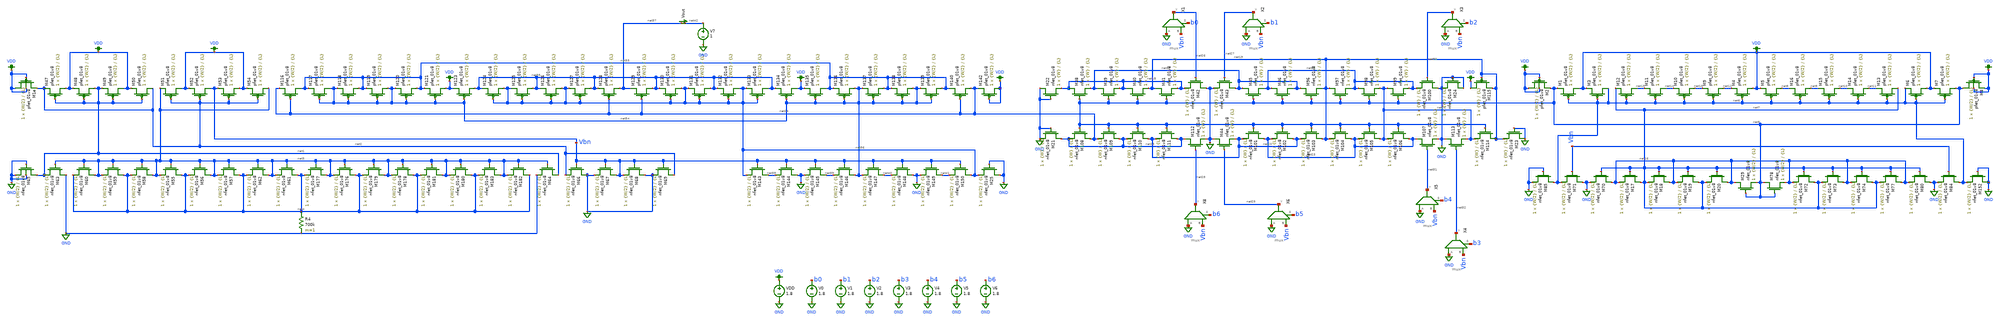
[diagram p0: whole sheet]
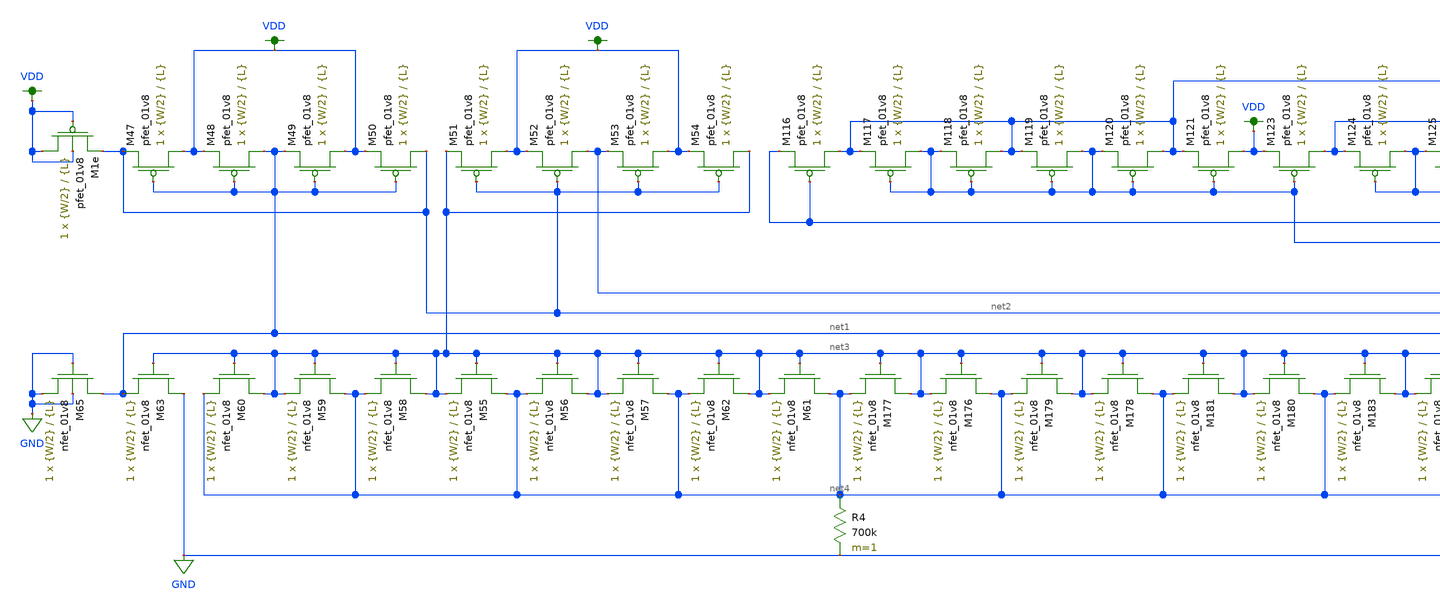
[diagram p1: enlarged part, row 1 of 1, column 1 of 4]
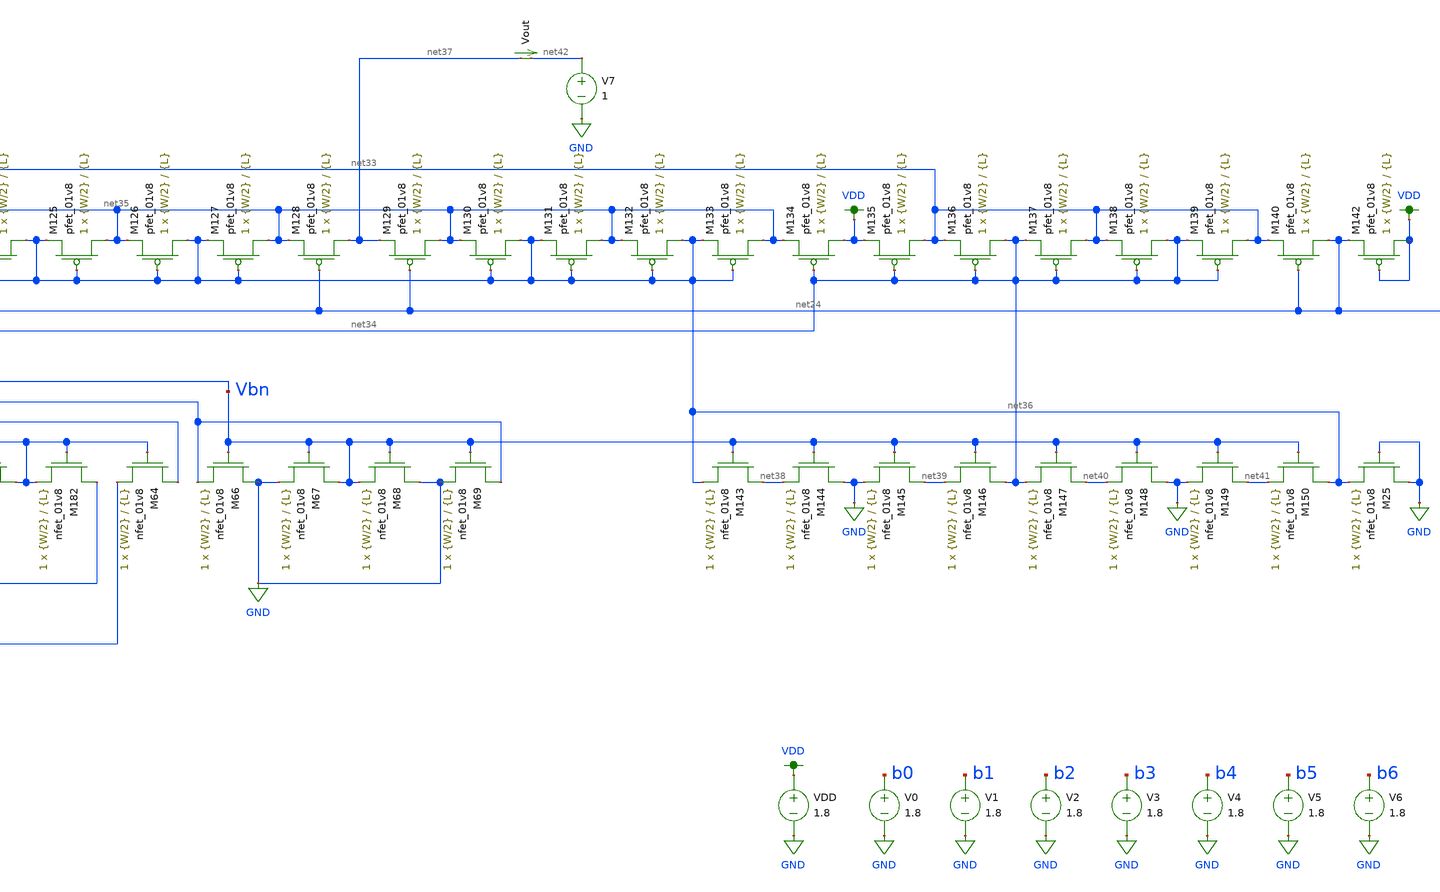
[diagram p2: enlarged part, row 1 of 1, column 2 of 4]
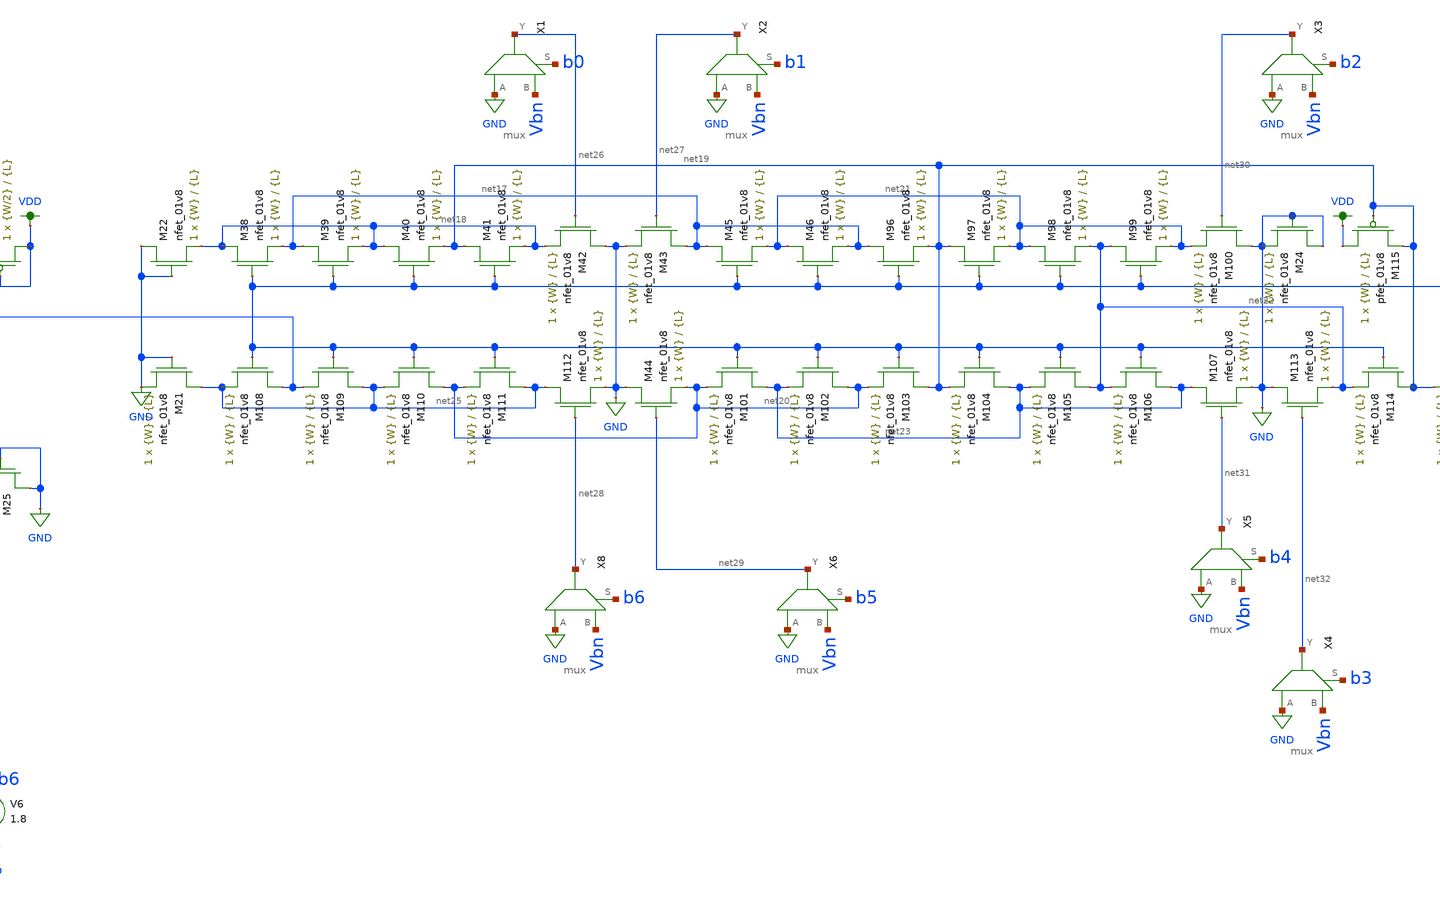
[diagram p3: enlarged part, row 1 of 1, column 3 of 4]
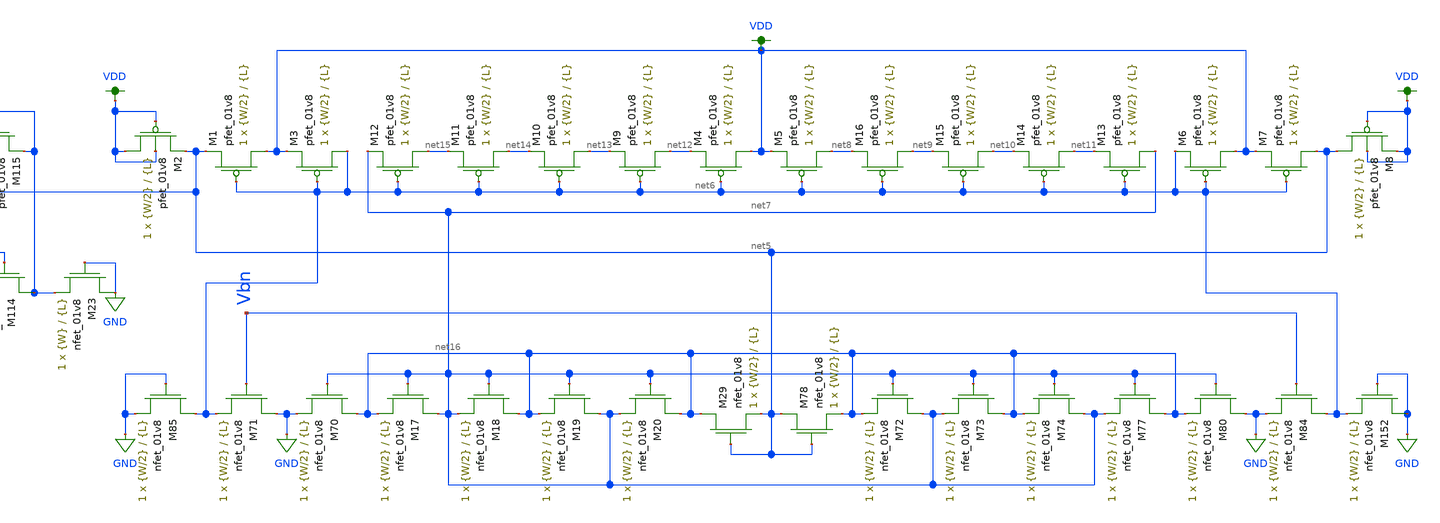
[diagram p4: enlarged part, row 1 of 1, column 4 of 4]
** sch_path: dac/schematics/LDS_FINAL.sch
**.subckt LDS_FINAL
V0 b0 GND 1.8
V1 b1 GND 1.8
V2 b2 GND 1.8
V3 b3 GND 1.8
V4 b4 GND 1.8
V5 b5 GND 1.8
V6 b6 GND 1.8
VDD VDD GND 1.8
XM47 VDD net1 net2 VDD sky130_fd_pr__pfet_01v8 L={L} W={W/2} nf=1 ad='int((nf+1)/2) * W/nf * 0.29' as='int((nf+2)/2) * W/nf * 0.29'
+ pd='2*int((nf+1)/2) * (W/nf + 0.29)' ps='2*int((nf+2)/2) * (W/nf + 0.29)' nrd='0.29 / W' nrs='0.29 / W'
+ sa=0 sb=0 sd=0 mult=1 m=1
XM48 net1 net1 VDD VDD sky130_fd_pr__pfet_01v8 L={L} W={W/2} nf=1 ad='int((nf+1)/2) * W/nf * 0.29' as='int((nf+2)/2) * W/nf * 0.29'
+ pd='2*int((nf+1)/2) * (W/nf + 0.29)' ps='2*int((nf+2)/2) * (W/nf + 0.29)' nrd='0.29 / W' nrs='0.29 / W'
+ sa=0 sb=0 sd=0 mult=1 m=1
XM49 VDD net1 net1 VDD sky130_fd_pr__pfet_01v8 L={L} W={W/2} nf=1 ad='int((nf+1)/2) * W/nf * 0.29' as='int((nf+2)/2) * W/nf * 0.29'
+ pd='2*int((nf+1)/2) * (W/nf + 0.29)' ps='2*int((nf+2)/2) * (W/nf + 0.29)' nrd='0.29 / W' nrs='0.29 / W'
+ sa=0 sb=0 sd=0 mult=1 m=1
XM50 net2 net1 VDD VDD sky130_fd_pr__pfet_01v8 L={L} W={W/2} nf=1 ad='int((nf+1)/2) * W/nf * 0.29' as='int((nf+2)/2) * W/nf * 0.29'
+ pd='2*int((nf+1)/2) * (W/nf + 0.29)' ps='2*int((nf+2)/2) * (W/nf + 0.29)' nrd='0.29 / W' nrs='0.29 / W'
+ sa=0 sb=0 sd=0 mult=1 m=1
XM51 VDD net2 net3 VDD sky130_fd_pr__pfet_01v8 L={L} W={W/2} nf=1 ad='int((nf+1)/2) * W/nf * 0.29' as='int((nf+2)/2) * W/nf * 0.29'
+ pd='2*int((nf+1)/2) * (W/nf + 0.29)' ps='2*int((nf+2)/2) * (W/nf + 0.29)' nrd='0.29 / W' nrs='0.29 / W'
+ sa=0 sb=0 sd=0 mult=1 m=1
XM52 Vbn net2 VDD VDD sky130_fd_pr__pfet_01v8 L={L} W={W/2} nf=1 ad='int((nf+1)/2) * W/nf * 0.29' as='int((nf+2)/2) * W/nf * 0.29'
+ pd='2*int((nf+1)/2) * (W/nf + 0.29)' ps='2*int((nf+2)/2) * (W/nf + 0.29)' nrd='0.29 / W' nrs='0.29 / W'
+ sa=0 sb=0 sd=0 mult=1 m=1
XM53 VDD net2 Vbn VDD sky130_fd_pr__pfet_01v8 L={L} W={W/2} nf=1 ad='int((nf+1)/2) * W/nf * 0.29' as='int((nf+2)/2) * W/nf * 0.29'
+ pd='2*int((nf+1)/2) * (W/nf + 0.29)' ps='2*int((nf+2)/2) * (W/nf + 0.29)' nrd='0.29 / W' nrs='0.29 / W'
+ sa=0 sb=0 sd=0 mult=1 m=1
XM54 net3 net2 VDD VDD sky130_fd_pr__pfet_01v8 L={L} W={W/2} nf=1 ad='int((nf+1)/2) * W/nf * 0.29' as='int((nf+2)/2) * W/nf * 0.29'
+ pd='2*int((nf+1)/2) * (W/nf + 0.29)' ps='2*int((nf+2)/2) * (W/nf + 0.29)' nrd='0.29 / W' nrs='0.29 / W'
+ sa=0 sb=0 sd=0 mult=1 m=1
XM55 net4 net3 net3 GND sky130_fd_pr__nfet_01v8 L={L} W={W/2} nf=1 ad='int((nf+1)/2) * W/nf * 0.29' as='int((nf+2)/2) * W/nf * 0.29'
+ pd='2*int((nf+1)/2) * (W/nf + 0.29)' ps='2*int((nf+2)/2) * (W/nf + 0.29)' nrd='0.29 / W' nrs='0.29 / W'
+ sa=0 sb=0 sd=0 mult=1 m=1
XM56 net3 net3 net4 GND sky130_fd_pr__nfet_01v8 L={L} W={W/2} nf=1 ad='int((nf+1)/2) * W/nf * 0.29' as='int((nf+2)/2) * W/nf * 0.29'
+ pd='2*int((nf+1)/2) * (W/nf + 0.29)' ps='2*int((nf+2)/2) * (W/nf + 0.29)' nrd='0.29 / W' nrs='0.29 / W'
+ sa=0 sb=0 sd=0 mult=1 m=1
XM57 net4 net3 net3 GND sky130_fd_pr__nfet_01v8 L={L} W={W/2} nf=1 ad='int((nf+1)/2) * W/nf * 0.29' as='int((nf+2)/2) * W/nf * 0.29'
+ pd='2*int((nf+1)/2) * (W/nf + 0.29)' ps='2*int((nf+2)/2) * (W/nf + 0.29)' nrd='0.29 / W' nrs='0.29 / W'
+ sa=0 sb=0 sd=0 mult=1 m=1
XM58 net3 net3 net4 GND sky130_fd_pr__nfet_01v8 L={L} W={W/2} nf=1 ad='int((nf+1)/2) * W/nf * 0.29' as='int((nf+2)/2) * W/nf * 0.29'
+ pd='2*int((nf+1)/2) * (W/nf + 0.29)' ps='2*int((nf+2)/2) * (W/nf + 0.29)' nrd='0.29 / W' nrs='0.29 / W'
+ sa=0 sb=0 sd=0 mult=1 m=1
XM59 net4 net3 net3 GND sky130_fd_pr__nfet_01v8 L={L} W={W/2} nf=1 ad='int((nf+1)/2) * W/nf * 0.29' as='int((nf+2)/2) * W/nf * 0.29'
+ pd='2*int((nf+1)/2) * (W/nf + 0.29)' ps='2*int((nf+2)/2) * (W/nf + 0.29)' nrd='0.29 / W' nrs='0.29 / W'
+ sa=0 sb=0 sd=0 mult=1 m=1
XM60 net3 net3 net4 GND sky130_fd_pr__nfet_01v8 L={L} W={W/2} nf=1 ad='int((nf+1)/2) * W/nf * 0.29' as='int((nf+2)/2) * W/nf * 0.29'
+ pd='2*int((nf+1)/2) * (W/nf + 0.29)' ps='2*int((nf+2)/2) * (W/nf + 0.29)' nrd='0.29 / W' nrs='0.29 / W'
+ sa=0 sb=0 sd=0 mult=1 m=1
XM61 net4 net3 net3 GND sky130_fd_pr__nfet_01v8 L={L} W={W/2} nf=1 ad='int((nf+1)/2) * W/nf * 0.29' as='int((nf+2)/2) * W/nf * 0.29'
+ pd='2*int((nf+1)/2) * (W/nf + 0.29)' ps='2*int((nf+2)/2) * (W/nf + 0.29)' nrd='0.29 / W' nrs='0.29 / W'
+ sa=0 sb=0 sd=0 mult=1 m=1
XM62 net3 net3 net4 GND sky130_fd_pr__nfet_01v8 L={L} W={W/2} nf=1 ad='int((nf+1)/2) * W/nf * 0.29' as='int((nf+2)/2) * W/nf * 0.29'
+ pd='2*int((nf+1)/2) * (W/nf + 0.29)' ps='2*int((nf+2)/2) * (W/nf + 0.29)' nrd='0.29 / W' nrs='0.29 / W'
+ sa=0 sb=0 sd=0 mult=1 m=1
XM63 GND net3 net1 GND sky130_fd_pr__nfet_01v8 L={L} W={W/2} nf=1 ad='int((nf+1)/2) * W/nf * 0.29' as='int((nf+2)/2) * W/nf * 0.29'
+ pd='2*int((nf+1)/2) * (W/nf + 0.29)' ps='2*int((nf+2)/2) * (W/nf + 0.29)' nrd='0.29 / W' nrs='0.29 / W'
+ sa=0 sb=0 sd=0 mult=1 m=1
XM64 net1 net3 GND GND sky130_fd_pr__nfet_01v8 L={L} W={W/2} nf=1 ad='int((nf+1)/2) * W/nf * 0.29' as='int((nf+2)/2) * W/nf * 0.29'
+ pd='2*int((nf+1)/2) * (W/nf + 0.29)' ps='2*int((nf+2)/2) * (W/nf + 0.29)' nrd='0.29 / W' nrs='0.29 / W'
+ sa=0 sb=0 sd=0 mult=1 m=1
R4 net4 GND 700k m=1
XM1e VDD VDD net2 VDD sky130_fd_pr__pfet_01v8 L={L} W={W/2} nf=1 ad='int((nf+1)/2) * W/nf * 0.29' as='int((nf+2)/2) * W/nf * 0.29'
+ pd='2*int((nf+1)/2) * (W/nf + 0.29)' ps='2*int((nf+2)/2) * (W/nf + 0.29)' nrd='0.29 / W' nrs='0.29 / W'
+ sa=0 sb=0 sd=0 mult=1 m=1
XM65 net1 GND GND GND sky130_fd_pr__nfet_01v8 L={L} W={W/2} nf=1 ad='int((nf+1)/2) * W/nf * 0.29' as='int((nf+2)/2) * W/nf * 0.29'
+ pd='2*int((nf+1)/2) * (W/nf + 0.29)' ps='2*int((nf+2)/2) * (W/nf + 0.29)' nrd='0.29 / W' nrs='0.29 / W'
+ sa=0 sb=0 sd=0 mult=1 m=1
XM66 GND Vbn net2 GND sky130_fd_pr__nfet_01v8 L={L} W={W/2} nf=1 ad='int((nf+1)/2) * W/nf * 0.29' as='int((nf+2)/2) * W/nf * 0.29'
+ pd='2*int((nf+1)/2) * (W/nf + 0.29)' ps='2*int((nf+2)/2) * (W/nf + 0.29)' nrd='0.29 / W' nrs='0.29 / W'
+ sa=0 sb=0 sd=0 mult=1 m=1
XM67 Vbn Vbn GND GND sky130_fd_pr__nfet_01v8 L={L} W={W/2} nf=1 ad='int((nf+1)/2) * W/nf * 0.29' as='int((nf+2)/2) * W/nf * 0.29'
+ pd='2*int((nf+1)/2) * (W/nf + 0.29)' ps='2*int((nf+2)/2) * (W/nf + 0.29)' nrd='0.29 / W' nrs='0.29 / W'
+ sa=0 sb=0 sd=0 mult=1 m=1
XM68 GND Vbn Vbn GND sky130_fd_pr__nfet_01v8 L={L} W={W/2} nf=1 ad='int((nf+1)/2) * W/nf * 0.29' as='int((nf+2)/2) * W/nf * 0.29'
+ pd='2*int((nf+1)/2) * (W/nf + 0.29)' ps='2*int((nf+2)/2) * (W/nf + 0.29)' nrd='0.29 / W' nrs='0.29 / W'
+ sa=0 sb=0 sd=0 mult=1 m=1
XM69 net2 Vbn GND GND sky130_fd_pr__nfet_01v8 L={L} W={W/2} nf=1 ad='int((nf+1)/2) * W/nf * 0.29' as='int((nf+2)/2) * W/nf * 0.29'
+ pd='2*int((nf+1)/2) * (W/nf + 0.29)' ps='2*int((nf+2)/2) * (W/nf + 0.29)' nrd='0.29 / W' nrs='0.29 / W'
+ sa=0 sb=0 sd=0 mult=1 m=1
XM176 net4 net3 net3 GND sky130_fd_pr__nfet_01v8 L={L} W={W/2} nf=1 ad='int((nf+1)/2) * W/nf * 0.29'
+ as='int((nf+2)/2) * W/nf * 0.29' pd='2*int((nf+1)/2) * (W/nf + 0.29)' ps='2*int((nf+2)/2) * (W/nf + 0.29)'
+ nrd='0.29 / W' nrs='0.29 / W' sa=0 sb=0 sd=0 mult=1 m=1
XM177 net3 net3 net4 GND sky130_fd_pr__nfet_01v8 L={L} W={W/2} nf=1 ad='int((nf+1)/2) * W/nf * 0.29'
+ as='int((nf+2)/2) * W/nf * 0.29' pd='2*int((nf+1)/2) * (W/nf + 0.29)' ps='2*int((nf+2)/2) * (W/nf + 0.29)'
+ nrd='0.29 / W' nrs='0.29 / W' sa=0 sb=0 sd=0 mult=1 m=1
XM178 net4 net3 net3 GND sky130_fd_pr__nfet_01v8 L={L} W={W/2} nf=1 ad='int((nf+1)/2) * W/nf * 0.29'
+ as='int((nf+2)/2) * W/nf * 0.29' pd='2*int((nf+1)/2) * (W/nf + 0.29)' ps='2*int((nf+2)/2) * (W/nf + 0.29)'
+ nrd='0.29 / W' nrs='0.29 / W' sa=0 sb=0 sd=0 mult=1 m=1
XM179 net3 net3 net4 GND sky130_fd_pr__nfet_01v8 L={L} W={W/2} nf=1 ad='int((nf+1)/2) * W/nf * 0.29'
+ as='int((nf+2)/2) * W/nf * 0.29' pd='2*int((nf+1)/2) * (W/nf + 0.29)' ps='2*int((nf+2)/2) * (W/nf + 0.29)'
+ nrd='0.29 / W' nrs='0.29 / W' sa=0 sb=0 sd=0 mult=1 m=1
XM180 net4 net3 net3 GND sky130_fd_pr__nfet_01v8 L={L} W={W/2} nf=1 ad='int((nf+1)/2) * W/nf * 0.29'
+ as='int((nf+2)/2) * W/nf * 0.29' pd='2*int((nf+1)/2) * (W/nf + 0.29)' ps='2*int((nf+2)/2) * (W/nf + 0.29)'
+ nrd='0.29 / W' nrs='0.29 / W' sa=0 sb=0 sd=0 mult=1 m=1
XM181 net3 net3 net4 GND sky130_fd_pr__nfet_01v8 L={L} W={W/2} nf=1 ad='int((nf+1)/2) * W/nf * 0.29'
+ as='int((nf+2)/2) * W/nf * 0.29' pd='2*int((nf+1)/2) * (W/nf + 0.29)' ps='2*int((nf+2)/2) * (W/nf + 0.29)'
+ nrd='0.29 / W' nrs='0.29 / W' sa=0 sb=0 sd=0 mult=1 m=1
XM182 net4 net3 net3 GND sky130_fd_pr__nfet_01v8 L={L} W={W/2} nf=1 ad='int((nf+1)/2) * W/nf * 0.29'
+ as='int((nf+2)/2) * W/nf * 0.29' pd='2*int((nf+1)/2) * (W/nf + 0.29)' ps='2*int((nf+2)/2) * (W/nf + 0.29)'
+ nrd='0.29 / W' nrs='0.29 / W' sa=0 sb=0 sd=0 mult=1 m=1
XM183 net3 net3 net4 GND sky130_fd_pr__nfet_01v8 L={L} W={W/2} nf=1 ad='int((nf+1)/2) * W/nf * 0.29'
+ as='int((nf+2)/2) * W/nf * 0.29' pd='2*int((nf+1)/2) * (W/nf + 0.29)' ps='2*int((nf+2)/2) * (W/nf + 0.29)'
+ nrd='0.29 / W' nrs='0.29 / W' sa=0 sb=0 sd=0 mult=1 m=1
XM1 VDD net6 net5 VDD sky130_fd_pr__pfet_01v8 L={L} W={W/2} nf=1 ad='int((nf+1)/2) * W/nf * 0.29' as='int((nf+2)/2) * W/nf * 0.29'
+ pd='2*int((nf+1)/2) * (W/nf + 0.29)' ps='2*int((nf+2)/2) * (W/nf + 0.29)' nrd='0.29 / W' nrs='0.29 / W'
+ sa=0 sb=0 sd=0 mult=1 m=1
XM2 VDD VDD net5 VDD sky130_fd_pr__pfet_01v8 L={L} W={W/2} nf=1 ad='int((nf+1)/2) * W/nf * 0.29' as='int((nf+2)/2) * W/nf * 0.29'
+ pd='2*int((nf+1)/2) * (W/nf + 0.29)' ps='2*int((nf+2)/2) * (W/nf + 0.29)' nrd='0.29 / W' nrs='0.29 / W'
+ sa=0 sb=0 sd=0 mult=1 m=1
XM3 net6 net6 VDD VDD sky130_fd_pr__pfet_01v8 L={L} W={W/2} nf=1 ad='int((nf+1)/2) * W/nf * 0.29' as='int((nf+2)/2) * W/nf * 0.29'
+ pd='2*int((nf+1)/2) * (W/nf + 0.29)' ps='2*int((nf+2)/2) * (W/nf + 0.29)' nrd='0.29 / W' nrs='0.29 / W'
+ sa=0 sb=0 sd=0 mult=1 m=1
XM4 VDD net6 net12 VDD sky130_fd_pr__pfet_01v8 L={L} W={W/2} nf=1 ad='int((nf+1)/2) * W/nf * 0.29' as='int((nf+2)/2) * W/nf * 0.29'
+ pd='2*int((nf+1)/2) * (W/nf + 0.29)' ps='2*int((nf+2)/2) * (W/nf + 0.29)' nrd='0.29 / W' nrs='0.29 / W'
+ sa=0 sb=0 sd=0 mult=1 m=1
XM5 net8 net6 VDD VDD sky130_fd_pr__pfet_01v8 L={L} W={W/2} nf=1 ad='int((nf+1)/2) * W/nf * 0.29' as='int((nf+2)/2) * W/nf * 0.29'
+ pd='2*int((nf+1)/2) * (W/nf + 0.29)' ps='2*int((nf+2)/2) * (W/nf + 0.29)' nrd='0.29 / W' nrs='0.29 / W'
+ sa=0 sb=0 sd=0 mult=1 m=1
XM6 VDD net6 net6 VDD sky130_fd_pr__pfet_01v8 L={L} W={W/2} nf=1 ad='int((nf+1)/2) * W/nf * 0.29' as='int((nf+2)/2) * W/nf * 0.29'
+ pd='2*int((nf+1)/2) * (W/nf + 0.29)' ps='2*int((nf+2)/2) * (W/nf + 0.29)' nrd='0.29 / W' nrs='0.29 / W'
+ sa=0 sb=0 sd=0 mult=1 m=1
XM7 net5 net6 VDD VDD sky130_fd_pr__pfet_01v8 L={L} W={W/2} nf=1 ad='int((nf+1)/2) * W/nf * 0.29' as='int((nf+2)/2) * W/nf * 0.29'
+ pd='2*int((nf+1)/2) * (W/nf + 0.29)' ps='2*int((nf+2)/2) * (W/nf + 0.29)' nrd='0.29 / W' nrs='0.29 / W'
+ sa=0 sb=0 sd=0 mult=1 m=1
XM8 net5 VDD VDD VDD sky130_fd_pr__pfet_01v8 L={L} W={W/2} nf=1 ad='int((nf+1)/2) * W/nf * 0.29' as='int((nf+2)/2) * W/nf * 0.29'
+ pd='2*int((nf+1)/2) * (W/nf + 0.29)' ps='2*int((nf+2)/2) * (W/nf + 0.29)' nrd='0.29 / W' nrs='0.29 / W'
+ sa=0 sb=0 sd=0 mult=1 m=1
XM9 net12 net6 net13 VDD sky130_fd_pr__pfet_01v8 L={L} W={W/2} nf=1 ad='int((nf+1)/2) * W/nf * 0.29'
+ as='int((nf+2)/2) * W/nf * 0.29' pd='2*int((nf+1)/2) * (W/nf + 0.29)' ps='2*int((nf+2)/2) * (W/nf + 0.29)'
+ nrd='0.29 / W' nrs='0.29 / W' sa=0 sb=0 sd=0 mult=1 m=1
XM10 net13 net6 net14 VDD sky130_fd_pr__pfet_01v8 L={L} W={W/2} nf=1 ad='int((nf+1)/2) * W/nf * 0.29'
+ as='int((nf+2)/2) * W/nf * 0.29' pd='2*int((nf+1)/2) * (W/nf + 0.29)' ps='2*int((nf+2)/2) * (W/nf + 0.29)'
+ nrd='0.29 / W' nrs='0.29 / W' sa=0 sb=0 sd=0 mult=1 m=1
XM11 net14 net6 net15 VDD sky130_fd_pr__pfet_01v8 L={L} W={W/2} nf=1 ad='int((nf+1)/2) * W/nf * 0.29'
+ as='int((nf+2)/2) * W/nf * 0.29' pd='2*int((nf+1)/2) * (W/nf + 0.29)' ps='2*int((nf+2)/2) * (W/nf + 0.29)'
+ nrd='0.29 / W' nrs='0.29 / W' sa=0 sb=0 sd=0 mult=1 m=1
XM12 net15 net6 net7 VDD sky130_fd_pr__pfet_01v8 L={L} W={W/2} nf=1 ad='int((nf+1)/2) * W/nf * 0.29'
+ as='int((nf+2)/2) * W/nf * 0.29' pd='2*int((nf+1)/2) * (W/nf + 0.29)' ps='2*int((nf+2)/2) * (W/nf + 0.29)'
+ nrd='0.29 / W' nrs='0.29 / W' sa=0 sb=0 sd=0 mult=1 m=1
XM13 net7 net6 net11 VDD sky130_fd_pr__pfet_01v8 L={L} W={W/2} nf=1 ad='int((nf+1)/2) * W/nf * 0.29'
+ as='int((nf+2)/2) * W/nf * 0.29' pd='2*int((nf+1)/2) * (W/nf + 0.29)' ps='2*int((nf+2)/2) * (W/nf + 0.29)'
+ nrd='0.29 / W' nrs='0.29 / W' sa=0 sb=0 sd=0 mult=1 m=1
XM14 net11 net6 net10 VDD sky130_fd_pr__pfet_01v8 L={L} W={W/2} nf=1 ad='int((nf+1)/2) * W/nf * 0.29'
+ as='int((nf+2)/2) * W/nf * 0.29' pd='2*int((nf+1)/2) * (W/nf + 0.29)' ps='2*int((nf+2)/2) * (W/nf + 0.29)'
+ nrd='0.29 / W' nrs='0.29 / W' sa=0 sb=0 sd=0 mult=1 m=1
XM15 net10 net6 net9 VDD sky130_fd_pr__pfet_01v8 L={L} W={W/2} nf=1 ad='int((nf+1)/2) * W/nf * 0.29'
+ as='int((nf+2)/2) * W/nf * 0.29' pd='2*int((nf+1)/2) * (W/nf + 0.29)' ps='2*int((nf+2)/2) * (W/nf + 0.29)'
+ nrd='0.29 / W' nrs='0.29 / W' sa=0 sb=0 sd=0 mult=1 m=1
XM16 net9 net6 net8 VDD sky130_fd_pr__pfet_01v8 L={L} W={W/2} nf=1 ad='int((nf+1)/2) * W/nf * 0.29' as='int((nf+2)/2) * W/nf * 0.29'
+ pd='2*int((nf+1)/2) * (W/nf + 0.29)' ps='2*int((nf+2)/2) * (W/nf + 0.29)' nrd='0.29 / W' nrs='0.29 / W'
+ sa=0 sb=0 sd=0 mult=1 m=1
XM17 net7 net7 net16 GND sky130_fd_pr__nfet_01v8 L={L} W={W/2} nf=1 ad='int((nf+1)/2) * W/nf * 0.29'
+ as='int((nf+2)/2) * W/nf * 0.29' pd='2*int((nf+1)/2) * (W/nf + 0.29)' ps='2*int((nf+2)/2) * (W/nf + 0.29)'
+ nrd='0.29 / W' nrs='0.29 / W' sa=0 sb=0 sd=0 mult=1 m=1
XM18 net16 net7 net7 GND sky130_fd_pr__nfet_01v8 L={L} W={W/2} nf=1 ad='int((nf+1)/2) * W/nf * 0.29'
+ as='int((nf+2)/2) * W/nf * 0.29' pd='2*int((nf+1)/2) * (W/nf + 0.29)' ps='2*int((nf+2)/2) * (W/nf + 0.29)'
+ nrd='0.29 / W' nrs='0.29 / W' sa=0 sb=0 sd=0 mult=1 m=1
XM19 net7 net7 net16 GND sky130_fd_pr__nfet_01v8 L={L} W={W/2} nf=1 ad='int((nf+1)/2) * W/nf * 0.29'
+ as='int((nf+2)/2) * W/nf * 0.29' pd='2*int((nf+1)/2) * (W/nf + 0.29)' ps='2*int((nf+2)/2) * (W/nf + 0.29)'
+ nrd='0.29 / W' nrs='0.29 / W' sa=0 sb=0 sd=0 mult=1 m=1
XM20 net16 net7 net7 GND sky130_fd_pr__nfet_01v8 L={L} W={W/2} nf=1 ad='int((nf+1)/2) * W/nf * 0.29'
+ as='int((nf+2)/2) * W/nf * 0.29' pd='2*int((nf+1)/2) * (W/nf + 0.29)' ps='2*int((nf+2)/2) * (W/nf + 0.29)'
+ nrd='0.29 / W' nrs='0.29 / W' sa=0 sb=0 sd=0 mult=1 m=1
XM29 net16 net5 net5 GND sky130_fd_pr__nfet_01v8 L={L} W={W/2} nf=1 ad='int((nf+1)/2) * W/nf * 0.29'
+ as='int((nf+2)/2) * W/nf * 0.29' pd='2*int((nf+1)/2) * (W/nf + 0.29)' ps='2*int((nf+2)/2) * (W/nf + 0.29)'
+ nrd='0.29 / W' nrs='0.29 / W' sa=0 sb=0 sd=0 mult=1 m=1
XM70 net16 net7 GND GND sky130_fd_pr__nfet_01v8 L={L} W={W/2} nf=1 ad='int((nf+1)/2) * W/nf * 0.29' as='int((nf+2)/2) * W/nf * 0.29'
+ pd='2*int((nf+1)/2) * (W/nf + 0.29)' ps='2*int((nf+2)/2) * (W/nf + 0.29)' nrd='0.29 / W' nrs='0.29 / W'
+ sa=0 sb=0 sd=0 mult=1 m=1
XM71 GND Vbn net6 GND sky130_fd_pr__nfet_01v8 L={L} W={W/2} nf=1 ad='int((nf+1)/2) * W/nf * 0.29' as='int((nf+2)/2) * W/nf * 0.29'
+ pd='2*int((nf+1)/2) * (W/nf + 0.29)' ps='2*int((nf+2)/2) * (W/nf + 0.29)' nrd='0.29 / W' nrs='0.29 / W'
+ sa=0 sb=0 sd=0 mult=1 m=1
XM72 net7 net7 net16 GND sky130_fd_pr__nfet_01v8 L={L} W={W/2} nf=1 ad='int((nf+1)/2) * W/nf * 0.29'
+ as='int((nf+2)/2) * W/nf * 0.29' pd='2*int((nf+1)/2) * (W/nf + 0.29)' ps='2*int((nf+2)/2) * (W/nf + 0.29)'
+ nrd='0.29 / W' nrs='0.29 / W' sa=0 sb=0 sd=0 mult=1 m=1
XM73 net16 net7 net7 GND sky130_fd_pr__nfet_01v8 L={L} W={W/2} nf=1 ad='int((nf+1)/2) * W/nf * 0.29'
+ as='int((nf+2)/2) * W/nf * 0.29' pd='2*int((nf+1)/2) * (W/nf + 0.29)' ps='2*int((nf+2)/2) * (W/nf + 0.29)'
+ nrd='0.29 / W' nrs='0.29 / W' sa=0 sb=0 sd=0 mult=1 m=1
XM74 net7 net7 net16 GND sky130_fd_pr__nfet_01v8 L={L} W={W/2} nf=1 ad='int((nf+1)/2) * W/nf * 0.29'
+ as='int((nf+2)/2) * W/nf * 0.29' pd='2*int((nf+1)/2) * (W/nf + 0.29)' ps='2*int((nf+2)/2) * (W/nf + 0.29)'
+ nrd='0.29 / W' nrs='0.29 / W' sa=0 sb=0 sd=0 mult=1 m=1
XM77 net16 net7 net7 GND sky130_fd_pr__nfet_01v8 L={L} W={W/2} nf=1 ad='int((nf+1)/2) * W/nf * 0.29'
+ as='int((nf+2)/2) * W/nf * 0.29' pd='2*int((nf+1)/2) * (W/nf + 0.29)' ps='2*int((nf+2)/2) * (W/nf + 0.29)'
+ nrd='0.29 / W' nrs='0.29 / W' sa=0 sb=0 sd=0 mult=1 m=1
XM78 net5 net5 net16 GND sky130_fd_pr__nfet_01v8 L={L} W={W/2} nf=1 ad='int((nf+1)/2) * W/nf * 0.29'
+ as='int((nf+2)/2) * W/nf * 0.29' pd='2*int((nf+1)/2) * (W/nf + 0.29)' ps='2*int((nf+2)/2) * (W/nf + 0.29)'
+ nrd='0.29 / W' nrs='0.29 / W' sa=0 sb=0 sd=0 mult=1 m=1
XM80 GND net7 net16 GND sky130_fd_pr__nfet_01v8 L={L} W={W/2} nf=1 ad='int((nf+1)/2) * W/nf * 0.29' as='int((nf+2)/2) * W/nf * 0.29'
+ pd='2*int((nf+1)/2) * (W/nf + 0.29)' ps='2*int((nf+2)/2) * (W/nf + 0.29)' nrd='0.29 / W' nrs='0.29 / W'
+ sa=0 sb=0 sd=0 mult=1 m=1
XM84 net6 Vbn GND GND sky130_fd_pr__nfet_01v8 L={L} W={W/2} nf=1 ad='int((nf+1)/2) * W/nf * 0.29' as='int((nf+2)/2) * W/nf * 0.29'
+ pd='2*int((nf+1)/2) * (W/nf + 0.29)' ps='2*int((nf+2)/2) * (W/nf + 0.29)' nrd='0.29 / W' nrs='0.29 / W'
+ sa=0 sb=0 sd=0 mult=1 m=1
XM85 net6 GND GND GND sky130_fd_pr__nfet_01v8 L={L} W={W/2} nf=1 ad='int((nf+1)/2) * W/nf * 0.29' as='int((nf+2)/2) * W/nf * 0.29'
+ pd='2*int((nf+1)/2) * (W/nf + 0.29)' ps='2*int((nf+2)/2) * (W/nf + 0.29)' nrd='0.29 / W' nrs='0.29 / W'
+ sa=0 sb=0 sd=0 mult=1 m=1
XM152 GND GND net6 GND sky130_fd_pr__nfet_01v8 L={L} W={W/2} nf=1 ad='int((nf+1)/2) * W/nf * 0.29' as='int((nf+2)/2) * W/nf * 0.29'
+ pd='2*int((nf+1)/2) * (W/nf + 0.29)' ps='2*int((nf+2)/2) * (W/nf + 0.29)' nrd='0.29 / W' nrs='0.29 / W'
+ sa=0 sb=0 sd=0 mult=1 m=1
X1 GND Vbn net26 b0 mux
X2 GND Vbn net27 b1 mux
X3 GND Vbn net30 b2 mux
X4 GND Vbn net32 b3 mux
X5 GND Vbn net31 b4 mux
X6 GND Vbn net29 b5 mux
X8 GND Vbn net28 b6 mux
XM38 net18 net5 net17 GND sky130_fd_pr__nfet_01v8 L={L} W={W} nf=1 ad='int((nf+1)/2) * W/nf * 0.29' as='int((nf+2)/2) * W/nf * 0.29'
+ pd='2*int((nf+1)/2) * (W/nf + 0.29)' ps='2*int((nf+2)/2) * (W/nf + 0.29)' nrd='0.29 / W' nrs='0.29 / W'
+ sa=0 sb=0 sd=0 mult=1 m=1
XM39 net17 net5 net18 GND sky130_fd_pr__nfet_01v8 L={L} W={W} nf=1 ad='int((nf+1)/2) * W/nf * 0.29' as='int((nf+2)/2) * W/nf * 0.29'
+ pd='2*int((nf+1)/2) * (W/nf + 0.29)' ps='2*int((nf+2)/2) * (W/nf + 0.29)' nrd='0.29 / W' nrs='0.29 / W'
+ sa=0 sb=0 sd=0 mult=1 m=1
XM40 net18 net5 net19 GND sky130_fd_pr__nfet_01v8 L={L} W={W} nf=1 ad='int((nf+1)/2) * W/nf * 0.29' as='int((nf+2)/2) * W/nf * 0.29'
+ pd='2*int((nf+1)/2) * (W/nf + 0.29)' ps='2*int((nf+2)/2) * (W/nf + 0.29)' nrd='0.29 / W' nrs='0.29 / W'
+ sa=0 sb=0 sd=0 mult=1 m=1
XM41 net19 net5 net18 GND sky130_fd_pr__nfet_01v8 L={L} W={W} nf=1 ad='int((nf+1)/2) * W/nf * 0.29' as='int((nf+2)/2) * W/nf * 0.29'
+ pd='2*int((nf+1)/2) * (W/nf + 0.29)' ps='2*int((nf+2)/2) * (W/nf + 0.29)' nrd='0.29 / W' nrs='0.29 / W'
+ sa=0 sb=0 sd=0 mult=1 m=1
XM42 GND net26 net18 GND sky130_fd_pr__nfet_01v8 L={L} W={W} nf=1 ad='int((nf+1)/2) * W/nf * 0.29' as='int((nf+2)/2) * W/nf * 0.29'
+ pd='2*int((nf+1)/2) * (W/nf + 0.29)' ps='2*int((nf+2)/2) * (W/nf + 0.29)' nrd='0.29 / W' nrs='0.29 / W'
+ sa=0 sb=0 sd=0 mult=1 m=1
XM43 net17 net27 GND GND sky130_fd_pr__nfet_01v8 L={L} W={W} nf=1 ad='int((nf+1)/2) * W/nf * 0.29' as='int((nf+2)/2) * W/nf * 0.29'
+ pd='2*int((nf+1)/2) * (W/nf + 0.29)' ps='2*int((nf+2)/2) * (W/nf + 0.29)' nrd='0.29 / W' nrs='0.29 / W'
+ sa=0 sb=0 sd=0 mult=1 m=1
XM44 GND net29 net20 GND sky130_fd_pr__nfet_01v8 L={L} W={W} nf=1 ad='int((nf+1)/2) * W/nf * 0.29' as='int((nf+2)/2) * W/nf * 0.29'
+ pd='2*int((nf+1)/2) * (W/nf + 0.29)' ps='2*int((nf+2)/2) * (W/nf + 0.29)' nrd='0.29 / W' nrs='0.29 / W'
+ sa=0 sb=0 sd=0 mult=1 m=1
XM45 net17 net5 net21 GND sky130_fd_pr__nfet_01v8 L={L} W={W} nf=1 ad='int((nf+1)/2) * W/nf * 0.29' as='int((nf+2)/2) * W/nf * 0.29'
+ pd='2*int((nf+1)/2) * (W/nf + 0.29)' ps='2*int((nf+2)/2) * (W/nf + 0.29)' nrd='0.29 / W' nrs='0.29 / W'
+ sa=0 sb=0 sd=0 mult=1 m=1
XM46 net21 net5 net17 GND sky130_fd_pr__nfet_01v8 L={L} W={W} nf=1 ad='int((nf+1)/2) * W/nf * 0.29' as='int((nf+2)/2) * W/nf * 0.29'
+ pd='2*int((nf+1)/2) * (W/nf + 0.29)' ps='2*int((nf+2)/2) * (W/nf + 0.29)' nrd='0.29 / W' nrs='0.29 / W'
+ sa=0 sb=0 sd=0 mult=1 m=1
XM96 net17 net5 net19 GND sky130_fd_pr__nfet_01v8 L={L} W={W} nf=1 ad='int((nf+1)/2) * W/nf * 0.29' as='int((nf+2)/2) * W/nf * 0.29'
+ pd='2*int((nf+1)/2) * (W/nf + 0.29)' ps='2*int((nf+2)/2) * (W/nf + 0.29)' nrd='0.29 / W' nrs='0.29 / W'
+ sa=0 sb=0 sd=0 mult=1 m=1
XM97 net19 net5 net21 GND sky130_fd_pr__nfet_01v8 L={L} W={W} nf=1 ad='int((nf+1)/2) * W/nf * 0.29' as='int((nf+2)/2) * W/nf * 0.29'
+ pd='2*int((nf+1)/2) * (W/nf + 0.29)' ps='2*int((nf+2)/2) * (W/nf + 0.29)' nrd='0.29 / W' nrs='0.29 / W'
+ sa=0 sb=0 sd=0 mult=1 m=1
XM98 net21 net5 net22 GND sky130_fd_pr__nfet_01v8 L={L} W={W} nf=1 ad='int((nf+1)/2) * W/nf * 0.29' as='int((nf+2)/2) * W/nf * 0.29'
+ pd='2*int((nf+1)/2) * (W/nf + 0.29)' ps='2*int((nf+2)/2) * (W/nf + 0.29)' nrd='0.29 / W' nrs='0.29 / W'
+ sa=0 sb=0 sd=0 mult=1 m=1
XM99 net22 net5 net21 GND sky130_fd_pr__nfet_01v8 L={L} W={W} nf=1 ad='int((nf+1)/2) * W/nf * 0.29' as='int((nf+2)/2) * W/nf * 0.29'
+ pd='2*int((nf+1)/2) * (W/nf + 0.29)' ps='2*int((nf+2)/2) * (W/nf + 0.29)' nrd='0.29 / W' nrs='0.29 / W'
+ sa=0 sb=0 sd=0 mult=1 m=1
XM100 GND net30 net21 GND sky130_fd_pr__nfet_01v8 L={L} W={W} nf=1 ad='int((nf+1)/2) * W/nf * 0.29' as='int((nf+2)/2) * W/nf * 0.29'
+ pd='2*int((nf+1)/2) * (W/nf + 0.29)' ps='2*int((nf+2)/2) * (W/nf + 0.29)' nrd='0.29 / W' nrs='0.29 / W'
+ sa=0 sb=0 sd=0 mult=1 m=1
XM101 net23 net5 net20 GND sky130_fd_pr__nfet_01v8 L={L} W={W} nf=1 ad='int((nf+1)/2) * W/nf * 0.29'
+ as='int((nf+2)/2) * W/nf * 0.29' pd='2*int((nf+1)/2) * (W/nf + 0.29)' ps='2*int((nf+2)/2) * (W/nf + 0.29)'
+ nrd='0.29 / W' nrs='0.29 / W' sa=0 sb=0 sd=0 mult=1 m=1
XM102 net20 net5 net23 GND sky130_fd_pr__nfet_01v8 L={L} W={W} nf=1 ad='int((nf+1)/2) * W/nf * 0.29'
+ as='int((nf+2)/2) * W/nf * 0.29' pd='2*int((nf+1)/2) * (W/nf + 0.29)' ps='2*int((nf+2)/2) * (W/nf + 0.29)'
+ nrd='0.29 / W' nrs='0.29 / W' sa=0 sb=0 sd=0 mult=1 m=1
XM103 net19 net5 net20 GND sky130_fd_pr__nfet_01v8 L={L} W={W} nf=1 ad='int((nf+1)/2) * W/nf * 0.29'
+ as='int((nf+2)/2) * W/nf * 0.29' pd='2*int((nf+1)/2) * (W/nf + 0.29)' ps='2*int((nf+2)/2) * (W/nf + 0.29)'
+ nrd='0.29 / W' nrs='0.29 / W' sa=0 sb=0 sd=0 mult=1 m=1
XM104 net23 net5 net19 GND sky130_fd_pr__nfet_01v8 L={L} W={W} nf=1 ad='int((nf+1)/2) * W/nf * 0.29'
+ as='int((nf+2)/2) * W/nf * 0.29' pd='2*int((nf+1)/2) * (W/nf + 0.29)' ps='2*int((nf+2)/2) * (W/nf + 0.29)'
+ nrd='0.29 / W' nrs='0.29 / W' sa=0 sb=0 sd=0 mult=1 m=1
XM105 net22 net5 net23 GND sky130_fd_pr__nfet_01v8 L={L} W={W} nf=1 ad='int((nf+1)/2) * W/nf * 0.29'
+ as='int((nf+2)/2) * W/nf * 0.29' pd='2*int((nf+1)/2) * (W/nf + 0.29)' ps='2*int((nf+2)/2) * (W/nf + 0.29)'
+ nrd='0.29 / W' nrs='0.29 / W' sa=0 sb=0 sd=0 mult=1 m=1
XM106 net23 net5 net22 GND sky130_fd_pr__nfet_01v8 L={L} W={W} nf=1 ad='int((nf+1)/2) * W/nf * 0.29'
+ as='int((nf+2)/2) * W/nf * 0.29' pd='2*int((nf+1)/2) * (W/nf + 0.29)' ps='2*int((nf+2)/2) * (W/nf + 0.29)'
+ nrd='0.29 / W' nrs='0.29 / W' sa=0 sb=0 sd=0 mult=1 m=1
XM107 net23 net31 GND GND sky130_fd_pr__nfet_01v8 L={L} W={W} nf=1 ad='int((nf+1)/2) * W/nf * 0.29' as='int((nf+2)/2) * W/nf * 0.29'
+ pd='2*int((nf+1)/2) * (W/nf + 0.29)' ps='2*int((nf+2)/2) * (W/nf + 0.29)' nrd='0.29 / W' nrs='0.29 / W'
+ sa=0 sb=0 sd=0 mult=1 m=1
XM108 net24 net5 net25 GND sky130_fd_pr__nfet_01v8 L={L} W={W} nf=1 ad='int((nf+1)/2) * W/nf * 0.29'
+ as='int((nf+2)/2) * W/nf * 0.29' pd='2*int((nf+1)/2) * (W/nf + 0.29)' ps='2*int((nf+2)/2) * (W/nf + 0.29)'
+ nrd='0.29 / W' nrs='0.29 / W' sa=0 sb=0 sd=0 mult=1 m=1
XM109 net25 net5 net24 GND sky130_fd_pr__nfet_01v8 L={L} W={W} nf=1 ad='int((nf+1)/2) * W/nf * 0.29'
+ as='int((nf+2)/2) * W/nf * 0.29' pd='2*int((nf+1)/2) * (W/nf + 0.29)' ps='2*int((nf+2)/2) * (W/nf + 0.29)'
+ nrd='0.29 / W' nrs='0.29 / W' sa=0 sb=0 sd=0 mult=1 m=1
XM110 net20 net5 net25 GND sky130_fd_pr__nfet_01v8 L={L} W={W} nf=1 ad='int((nf+1)/2) * W/nf * 0.29'
+ as='int((nf+2)/2) * W/nf * 0.29' pd='2*int((nf+1)/2) * (W/nf + 0.29)' ps='2*int((nf+2)/2) * (W/nf + 0.29)'
+ nrd='0.29 / W' nrs='0.29 / W' sa=0 sb=0 sd=0 mult=1 m=1
XM111 net25 net5 net20 GND sky130_fd_pr__nfet_01v8 L={L} W={W} nf=1 ad='int((nf+1)/2) * W/nf * 0.29'
+ as='int((nf+2)/2) * W/nf * 0.29' pd='2*int((nf+1)/2) * (W/nf + 0.29)' ps='2*int((nf+2)/2) * (W/nf + 0.29)'
+ nrd='0.29 / W' nrs='0.29 / W' sa=0 sb=0 sd=0 mult=1 m=1
XM112 net25 net28 GND GND sky130_fd_pr__nfet_01v8 L={L} W={W} nf=1 ad='int((nf+1)/2) * W/nf * 0.29' as='int((nf+2)/2) * W/nf * 0.29'
+ pd='2*int((nf+1)/2) * (W/nf + 0.29)' ps='2*int((nf+2)/2) * (W/nf + 0.29)' nrd='0.29 / W' nrs='0.29 / W'
+ sa=0 sb=0 sd=0 mult=1 m=1
XM113 GND net32 net22 GND sky130_fd_pr__nfet_01v8 L={L} W={W} nf=1 ad='int((nf+1)/2) * W/nf * 0.29' as='int((nf+2)/2) * W/nf * 0.29'
+ pd='2*int((nf+1)/2) * (W/nf + 0.29)' ps='2*int((nf+2)/2) * (W/nf + 0.29)' nrd='0.29 / W' nrs='0.29 / W'
+ sa=0 sb=0 sd=0 mult=1 m=1
XM114 net19 net5 net22 GND sky130_fd_pr__nfet_01v8 L={L} W={W} nf=1 ad='int((nf+1)/2) * W/nf * 0.29'
+ as='int((nf+2)/2) * W/nf * 0.29' pd='2*int((nf+1)/2) * (W/nf + 0.29)' ps='2*int((nf+2)/2) * (W/nf + 0.29)'
+ nrd='0.29 / W' nrs='0.29 / W' sa=0 sb=0 sd=0 mult=1 m=1
XM115 VDD net19 net19 VDD sky130_fd_pr__pfet_01v8 L={L} W={W} nf=1 ad='int((nf+1)/2) * W/nf * 0.29' as='int((nf+2)/2) * W/nf * 0.29'
+ pd='2*int((nf+1)/2) * (W/nf + 0.29)' ps='2*int((nf+2)/2) * (W/nf + 0.29)' nrd='0.29 / W' nrs='0.29 / W'
+ sa=0 sb=0 sd=0 mult=1 m=1
XM116 net33 net24 net24 VDD sky130_fd_pr__pfet_01v8 L={L} W={W/2} nf=1 ad='int((nf+1)/2) * W/nf * 0.29'
+ as='int((nf+2)/2) * W/nf * 0.29' pd='2*int((nf+1)/2) * (W/nf + 0.29)' ps='2*int((nf+2)/2) * (W/nf + 0.29)'
+ nrd='0.29 / W' nrs='0.29 / W' sa=0 sb=0 sd=0 mult=1 m=1
XM117 net34 net34 net33 VDD sky130_fd_pr__pfet_01v8 L={L} W={W/2} nf=1 ad='int((nf+1)/2) * W/nf * 0.29'
+ as='int((nf+2)/2) * W/nf * 0.29' pd='2*int((nf+1)/2) * (W/nf + 0.29)' ps='2*int((nf+2)/2) * (W/nf + 0.29)'
+ nrd='0.29 / W' nrs='0.29 / W' sa=0 sb=0 sd=0 mult=1 m=1
XM118 net33 net34 net34 VDD sky130_fd_pr__pfet_01v8 L={L} W={W/2} nf=1 ad='int((nf+1)/2) * W/nf * 0.29'
+ as='int((nf+2)/2) * W/nf * 0.29' pd='2*int((nf+1)/2) * (W/nf + 0.29)' ps='2*int((nf+2)/2) * (W/nf + 0.29)'
+ nrd='0.29 / W' nrs='0.29 / W' sa=0 sb=0 sd=0 mult=1 m=1
XM119 net34 net34 net33 VDD sky130_fd_pr__pfet_01v8 L={L} W={W/2} nf=1 ad='int((nf+1)/2) * W/nf * 0.29'
+ as='int((nf+2)/2) * W/nf * 0.29' pd='2*int((nf+1)/2) * (W/nf + 0.29)' ps='2*int((nf+2)/2) * (W/nf + 0.29)'
+ nrd='0.29 / W' nrs='0.29 / W' sa=0 sb=0 sd=0 mult=1 m=1
XM120 net33 net34 net34 VDD sky130_fd_pr__pfet_01v8 L={L} W={W/2} nf=1 ad='int((nf+1)/2) * W/nf * 0.29'
+ as='int((nf+2)/2) * W/nf * 0.29' pd='2*int((nf+1)/2) * (W/nf + 0.29)' ps='2*int((nf+2)/2) * (W/nf + 0.29)'
+ nrd='0.29 / W' nrs='0.29 / W' sa=0 sb=0 sd=0 mult=1 m=1
XM121 VDD net34 net33 VDD sky130_fd_pr__pfet_01v8 L={L} W={W/2} nf=1 ad='int((nf+1)/2) * W/nf * 0.29'
+ as='int((nf+2)/2) * W/nf * 0.29' pd='2*int((nf+1)/2) * (W/nf + 0.29)' ps='2*int((nf+2)/2) * (W/nf + 0.29)'
+ nrd='0.29 / W' nrs='0.29 / W' sa=0 sb=0 sd=0 mult=1 m=1
XM123 net35 net34 VDD VDD sky130_fd_pr__pfet_01v8 L={L} W={W/2} nf=1 ad='int((nf+1)/2) * W/nf * 0.29'
+ as='int((nf+2)/2) * W/nf * 0.29' pd='2*int((nf+1)/2) * (W/nf + 0.29)' ps='2*int((nf+2)/2) * (W/nf + 0.29)'
+ nrd='0.29 / W' nrs='0.29 / W' sa=0 sb=0 sd=0 mult=1 m=1
XM124 net36 net36 net35 VDD sky130_fd_pr__pfet_01v8 L={L} W={W/2} nf=1 ad='int((nf+1)/2) * W/nf * 0.29'
+ as='int((nf+2)/2) * W/nf * 0.29' pd='2*int((nf+1)/2) * (W/nf + 0.29)' ps='2*int((nf+2)/2) * (W/nf + 0.29)'
+ nrd='0.29 / W' nrs='0.29 / W' sa=0 sb=0 sd=0 mult=1 m=1
XM125 net35 net36 net36 VDD sky130_fd_pr__pfet_01v8 L={L} W={W/2} nf=1 ad='int((nf+1)/2) * W/nf * 0.29'
+ as='int((nf+2)/2) * W/nf * 0.29' pd='2*int((nf+1)/2) * (W/nf + 0.29)' ps='2*int((nf+2)/2) * (W/nf + 0.29)'
+ nrd='0.29 / W' nrs='0.29 / W' sa=0 sb=0 sd=0 mult=1 m=1
XM126 net36 net36 net35 VDD sky130_fd_pr__pfet_01v8 L={L} W={W/2} nf=1 ad='int((nf+1)/2) * W/nf * 0.29'
+ as='int((nf+2)/2) * W/nf * 0.29' pd='2*int((nf+1)/2) * (W/nf + 0.29)' ps='2*int((nf+2)/2) * (W/nf + 0.29)'
+ nrd='0.29 / W' nrs='0.29 / W' sa=0 sb=0 sd=0 mult=1 m=1
XM127 net35 net36 net36 VDD sky130_fd_pr__pfet_01v8 L={L} W={W/2} nf=1 ad='int((nf+1)/2) * W/nf * 0.29'
+ as='int((nf+2)/2) * W/nf * 0.29' pd='2*int((nf+1)/2) * (W/nf + 0.29)' ps='2*int((nf+2)/2) * (W/nf + 0.29)'
+ nrd='0.29 / W' nrs='0.29 / W' sa=0 sb=0 sd=0 mult=1 m=1
XM128 net37 net24 net35 VDD sky130_fd_pr__pfet_01v8 L={L} W={W/2} nf=1 ad='int((nf+1)/2) * W/nf * 0.29'
+ as='int((nf+2)/2) * W/nf * 0.29' pd='2*int((nf+1)/2) * (W/nf + 0.29)' ps='2*int((nf+2)/2) * (W/nf + 0.29)'
+ nrd='0.29 / W' nrs='0.29 / W' sa=0 sb=0 sd=0 mult=1 m=1
XM129 net35 net24 net37 VDD sky130_fd_pr__pfet_01v8 L={L} W={W/2} nf=1 ad='int((nf+1)/2) * W/nf * 0.29'
+ as='int((nf+2)/2) * W/nf * 0.29' pd='2*int((nf+1)/2) * (W/nf + 0.29)' ps='2*int((nf+2)/2) * (W/nf + 0.29)'
+ nrd='0.29 / W' nrs='0.29 / W' sa=0 sb=0 sd=0 mult=1 m=1
XM130 net36 net36 net35 VDD sky130_fd_pr__pfet_01v8 L={L} W={W/2} nf=1 ad='int((nf+1)/2) * W/nf * 0.29'
+ as='int((nf+2)/2) * W/nf * 0.29' pd='2*int((nf+1)/2) * (W/nf + 0.29)' ps='2*int((nf+2)/2) * (W/nf + 0.29)'
+ nrd='0.29 / W' nrs='0.29 / W' sa=0 sb=0 sd=0 mult=1 m=1
XM131 net35 net36 net36 VDD sky130_fd_pr__pfet_01v8 L={L} W={W/2} nf=1 ad='int((nf+1)/2) * W/nf * 0.29'
+ as='int((nf+2)/2) * W/nf * 0.29' pd='2*int((nf+1)/2) * (W/nf + 0.29)' ps='2*int((nf+2)/2) * (W/nf + 0.29)'
+ nrd='0.29 / W' nrs='0.29 / W' sa=0 sb=0 sd=0 mult=1 m=1
XM132 net36 net36 net35 VDD sky130_fd_pr__pfet_01v8 L={L} W={W/2} nf=1 ad='int((nf+1)/2) * W/nf * 0.29'
+ as='int((nf+2)/2) * W/nf * 0.29' pd='2*int((nf+1)/2) * (W/nf + 0.29)' ps='2*int((nf+2)/2) * (W/nf + 0.29)'
+ nrd='0.29 / W' nrs='0.29 / W' sa=0 sb=0 sd=0 mult=1 m=1
XM133 net35 net36 net36 VDD sky130_fd_pr__pfet_01v8 L={L} W={W/2} nf=1 ad='int((nf+1)/2) * W/nf * 0.29'
+ as='int((nf+2)/2) * W/nf * 0.29' pd='2*int((nf+1)/2) * (W/nf + 0.29)' ps='2*int((nf+2)/2) * (W/nf + 0.29)'
+ nrd='0.29 / W' nrs='0.29 / W' sa=0 sb=0 sd=0 mult=1 m=1
XM134 VDD net34 net35 VDD sky130_fd_pr__pfet_01v8 L={L} W={W/2} nf=1 ad='int((nf+1)/2) * W/nf * 0.29'
+ as='int((nf+2)/2) * W/nf * 0.29' pd='2*int((nf+1)/2) * (W/nf + 0.29)' ps='2*int((nf+2)/2) * (W/nf + 0.29)'
+ nrd='0.29 / W' nrs='0.29 / W' sa=0 sb=0 sd=0 mult=1 m=1
XM135 net33 net34 VDD VDD sky130_fd_pr__pfet_01v8 L={L} W={W/2} nf=1 ad='int((nf+1)/2) * W/nf * 0.29'
+ as='int((nf+2)/2) * W/nf * 0.29' pd='2*int((nf+1)/2) * (W/nf + 0.29)' ps='2*int((nf+2)/2) * (W/nf + 0.29)'
+ nrd='0.29 / W' nrs='0.29 / W' sa=0 sb=0 sd=0 mult=1 m=1
XM136 net34 net34 net33 VDD sky130_fd_pr__pfet_01v8 L={L} W={W/2} nf=1 ad='int((nf+1)/2) * W/nf * 0.29'
+ as='int((nf+2)/2) * W/nf * 0.29' pd='2*int((nf+1)/2) * (W/nf + 0.29)' ps='2*int((nf+2)/2) * (W/nf + 0.29)'
+ nrd='0.29 / W' nrs='0.29 / W' sa=0 sb=0 sd=0 mult=1 m=1
XM137 net33 net34 net34 VDD sky130_fd_pr__pfet_01v8 L={L} W={W/2} nf=1 ad='int((nf+1)/2) * W/nf * 0.29'
+ as='int((nf+2)/2) * W/nf * 0.29' pd='2*int((nf+1)/2) * (W/nf + 0.29)' ps='2*int((nf+2)/2) * (W/nf + 0.29)'
+ nrd='0.29 / W' nrs='0.29 / W' sa=0 sb=0 sd=0 mult=1 m=1
XM138 net34 net34 net33 VDD sky130_fd_pr__pfet_01v8 L={L} W={W/2} nf=1 ad='int((nf+1)/2) * W/nf * 0.29'
+ as='int((nf+2)/2) * W/nf * 0.29' pd='2*int((nf+1)/2) * (W/nf + 0.29)' ps='2*int((nf+2)/2) * (W/nf + 0.29)'
+ nrd='0.29 / W' nrs='0.29 / W' sa=0 sb=0 sd=0 mult=1 m=1
XM139 net33 net34 net34 VDD sky130_fd_pr__pfet_01v8 L={L} W={W/2} nf=1 ad='int((nf+1)/2) * W/nf * 0.29'
+ as='int((nf+2)/2) * W/nf * 0.29' pd='2*int((nf+1)/2) * (W/nf + 0.29)' ps='2*int((nf+2)/2) * (W/nf + 0.29)'
+ nrd='0.29 / W' nrs='0.29 / W' sa=0 sb=0 sd=0 mult=1 m=1
XM140 net24 net24 net33 VDD sky130_fd_pr__pfet_01v8 L={L} W={W/2} nf=1 ad='int((nf+1)/2) * W/nf * 0.29'
+ as='int((nf+2)/2) * W/nf * 0.29' pd='2*int((nf+1)/2) * (W/nf + 0.29)' ps='2*int((nf+2)/2) * (W/nf + 0.29)'
+ nrd='0.29 / W' nrs='0.29 / W' sa=0 sb=0 sd=0 mult=1 m=1
XM142 VDD VDD net24 VDD sky130_fd_pr__pfet_01v8 L={L} W={W/2} nf=1 ad='int((nf+1)/2) * W/nf * 0.29' as='int((nf+2)/2) * W/nf * 0.29'
+ pd='2*int((nf+1)/2) * (W/nf + 0.29)' ps='2*int((nf+2)/2) * (W/nf + 0.29)' nrd='0.29 / W' nrs='0.29 / W'
+ sa=0 sb=0 sd=0 mult=1 m=1
XM143 net38 Vbn net36 GND sky130_fd_pr__nfet_01v8 L={L} W={W/2} nf=1 ad='int((nf+1)/2) * W/nf * 0.29'
+ as='int((nf+2)/2) * W/nf * 0.29' pd='2*int((nf+1)/2) * (W/nf + 0.29)' ps='2*int((nf+2)/2) * (W/nf + 0.29)'
+ nrd='0.29 / W' nrs='0.29 / W' sa=0 sb=0 sd=0 mult=1 m=1
XM144 GND Vbn net38 GND sky130_fd_pr__nfet_01v8 L={L} W={W/2} nf=1 ad='int((nf+1)/2) * W/nf * 0.29' as='int((nf+2)/2) * W/nf * 0.29'
+ pd='2*int((nf+1)/2) * (W/nf + 0.29)' ps='2*int((nf+2)/2) * (W/nf + 0.29)' nrd='0.29 / W' nrs='0.29 / W'
+ sa=0 sb=0 sd=0 mult=1 m=1
XM145 net39 Vbn GND GND sky130_fd_pr__nfet_01v8 L={L} W={W/2} nf=1 ad='int((nf+1)/2) * W/nf * 0.29' as='int((nf+2)/2) * W/nf * 0.29'
+ pd='2*int((nf+1)/2) * (W/nf + 0.29)' ps='2*int((nf+2)/2) * (W/nf + 0.29)' nrd='0.29 / W' nrs='0.29 / W'
+ sa=0 sb=0 sd=0 mult=1 m=1
XM146 net34 Vbn net39 GND sky130_fd_pr__nfet_01v8 L={L} W={W/2} nf=1 ad='int((nf+1)/2) * W/nf * 0.29'
+ as='int((nf+2)/2) * W/nf * 0.29' pd='2*int((nf+1)/2) * (W/nf + 0.29)' ps='2*int((nf+2)/2) * (W/nf + 0.29)'
+ nrd='0.29 / W' nrs='0.29 / W' sa=0 sb=0 sd=0 mult=1 m=1
XM147 net40 Vbn net34 GND sky130_fd_pr__nfet_01v8 L={L} W={W/2} nf=1 ad='int((nf+1)/2) * W/nf * 0.29'
+ as='int((nf+2)/2) * W/nf * 0.29' pd='2*int((nf+1)/2) * (W/nf + 0.29)' ps='2*int((nf+2)/2) * (W/nf + 0.29)'
+ nrd='0.29 / W' nrs='0.29 / W' sa=0 sb=0 sd=0 mult=1 m=1
XM148 GND Vbn net40 GND sky130_fd_pr__nfet_01v8 L={L} W={W/2} nf=1 ad='int((nf+1)/2) * W/nf * 0.29' as='int((nf+2)/2) * W/nf * 0.29'
+ pd='2*int((nf+1)/2) * (W/nf + 0.29)' ps='2*int((nf+2)/2) * (W/nf + 0.29)' nrd='0.29 / W' nrs='0.29 / W'
+ sa=0 sb=0 sd=0 mult=1 m=1
XM149 net41 Vbn GND GND sky130_fd_pr__nfet_01v8 L={L} W={W/2} nf=1 ad='int((nf+1)/2) * W/nf * 0.29' as='int((nf+2)/2) * W/nf * 0.29'
+ pd='2*int((nf+1)/2) * (W/nf + 0.29)' ps='2*int((nf+2)/2) * (W/nf + 0.29)' nrd='0.29 / W' nrs='0.29 / W'
+ sa=0 sb=0 sd=0 mult=1 m=1
XM150 net36 Vbn net41 GND sky130_fd_pr__nfet_01v8 L={L} W={W/2} nf=1 ad='int((nf+1)/2) * W/nf * 0.29'
+ as='int((nf+2)/2) * W/nf * 0.29' pd='2*int((nf+1)/2) * (W/nf + 0.29)' ps='2*int((nf+2)/2) * (W/nf + 0.29)'
+ nrd='0.29 / W' nrs='0.29 / W' sa=0 sb=0 sd=0 mult=1 m=1
Vout net37 net42 0
.save i(vout)
XM21 net25 GND GND GND sky130_fd_pr__nfet_01v8 L={L} W={W} nf=1 ad='int((nf+1)/2) * W/nf * 0.29' as='int((nf+2)/2) * W/nf * 0.29'
+ pd='2*int((nf+1)/2) * (W/nf + 0.29)' ps='2*int((nf+2)/2) * (W/nf + 0.29)' nrd='0.29 / W' nrs='0.29 / W'
+ sa=0 sb=0 sd=0 mult=1 m=1
XM22 GND GND net18 GND sky130_fd_pr__nfet_01v8 L={L} W={W} nf=1 ad='int((nf+1)/2) * W/nf * 0.29' as='int((nf+2)/2) * W/nf * 0.29'
+ pd='2*int((nf+1)/2) * (W/nf + 0.29)' ps='2*int((nf+2)/2) * (W/nf + 0.29)' nrd='0.29 / W' nrs='0.29 / W'
+ sa=0 sb=0 sd=0 mult=1 m=1
XM23 GND GND net19 GND sky130_fd_pr__nfet_01v8 L={L} W={W} nf=1 ad='int((nf+1)/2) * W/nf * 0.29' as='int((nf+2)/2) * W/nf * 0.29'
+ pd='2*int((nf+1)/2) * (W/nf + 0.29)' ps='2*int((nf+2)/2) * (W/nf + 0.29)' nrd='0.29 / W' nrs='0.29 / W'
+ sa=0 sb=0 sd=0 mult=1 m=1
XM24 GND GND GND GND sky130_fd_pr__nfet_01v8 L={L} W={W} nf=1 ad='int((nf+1)/2) * W/nf * 0.29' as='int((nf+2)/2) * W/nf * 0.29'
+ pd='2*int((nf+1)/2) * (W/nf + 0.29)' ps='2*int((nf+2)/2) * (W/nf + 0.29)' nrd='0.29 / W' nrs='0.29 / W'
+ sa=0 sb=0 sd=0 mult=1 m=1
V7 net42 GND 1
XM25 GND GND net36 GND sky130_fd_pr__nfet_01v8 L={L} W={W/2} nf=1 ad='int((nf+1)/2) * W/nf * 0.29' as='int((nf+2)/2) * W/nf * 0.29'
+ pd='2*int((nf+1)/2) * (W/nf + 0.29)' ps='2*int((nf+2)/2) * (W/nf + 0.29)' nrd='0.29 / W' nrs='0.29 / W'
+ sa=0 sb=0 sd=0 mult=1 m=1
**** begin user architecture code

.param W=24
.param L=1
.control
set wr_vecnames
set wr_singlescale
let code = 0
  while code < 128
    if code eq 0
      let b0 = 0
    else
      let b0 = code % 2 * 1.8
    end
    if floor(code / 2) eq 0
      let b1 = 0
    else
      let b1 = floor(code / 2) % 2 * 1.8
    end
    if floor(code / 4) eq 0
      let b2 = 0
    else
      let b2 = floor(code / 4) % 2 * 1.8
    end
    if floor(code / 8) eq 0
      let b3 = 0
    else
      let b3 = floor(code / 8) % 2 * 1.8
    end
    if floor(code / 16) eq 0
      let b4 = 0
    else
      let b4 = floor(code / 16) % 2 * 1.8
    end
    if floor(code / 32) eq 0
      let b5 = 0
    else
      let b5 = floor(code / 32) % 2 * 1.8
    end
    if floor(code / 64) eq 0
      let b6 = 0
    else
      let b6 = floor(code / 64) % 2 * 1.8
    end
    alter v0 $&b0
    alter v1 $&b1
    alter v2 $&b2
    alter v3 $&b3
    alter v4 $&b4
    alter v5 $&b5
    alter v6 $&b6
    save all
    op
    wrdata ~/Documents/current-output-dac-vlsi/simulations/dac_sim.txt i(Vout)
    if code eq 0
      set appendwrite
      set wr_vecnames = FALSE
    end
    let code = code + 1
  end
.endc


.option wnflag=1
.param MC_SWITCH=0.0
.lib ~/skywater/skywater-pdk/libraries/sky130_fd_pr_ngspice/latest/models/sky130.lib.spice tt

**** end user architecture code
**.ends

* expanding   symbol:  /home/madvlsi/Documents/current-output-dac-vlsi/schematics/mux.sym # of
*+ pins=4
** sym_path: dac/schematics/mux.sym
** sch_path: dac/schematics/mux.sch
.subckt mux A B Y S
*.ipin A
*.ipin B
*.ipin S
*.opin Y
XM1 A S Y VDD sky130_fd_pr__pfet_01v8 L=0.15 W=1 nf=1 ad='int((nf+1)/2) * W/nf * 0.29' as='int((nf+2)/2) * W/nf * 0.29'
+ pd='2*int((nf+1)/2) * (W/nf + 0.29)' ps='2*int((nf+2)/2) * (W/nf + 0.29)' nrd='0.29 / W' nrs='0.29 / W'
+ sa=0 sb=0 sd=0 mult=1 m=1
XM3 net1 S VDD VDD sky130_fd_pr__pfet_01v8 L=0.15 W=1 nf=1 ad='int((nf+1)/2) * W/nf * 0.29' as='int((nf+2)/2) * W/nf * 0.29'
+ pd='2*int((nf+1)/2) * (W/nf + 0.29)' ps='2*int((nf+2)/2) * (W/nf + 0.29)' nrd='0.29 / W' nrs='0.29 / W'
+ sa=0 sb=0 sd=0 mult=1 m=1
XM4 net1 S GND GND sky130_fd_pr__nfet_01v8 L=0.15 W=1 nf=1 ad='int((nf+1)/2) * W/nf * 0.29' as='int((nf+2)/2) * W/nf * 0.29'
+ pd='2*int((nf+1)/2) * (W/nf + 0.29)' ps='2*int((nf+2)/2) * (W/nf + 0.29)' nrd='0.29 / W' nrs='0.29 / W'
+ sa=0 sb=0 sd=0 mult=1 m=1
XM5 A net1 Y GND sky130_fd_pr__nfet_01v8 L=0.15 W=1 nf=1 ad='int((nf+1)/2) * W/nf * 0.29' as='int((nf+2)/2) * W/nf * 0.29'
+ pd='2*int((nf+1)/2) * (W/nf + 0.29)' ps='2*int((nf+2)/2) * (W/nf + 0.29)' nrd='0.29 / W' nrs='0.29 / W'
+ sa=0 sb=0 sd=0 mult=1 m=1
XM2 B net1 Y VDD sky130_fd_pr__pfet_01v8 L=0.15 W=1 nf=1 ad='int((nf+1)/2) * W/nf * 0.29' as='int((nf+2)/2) * W/nf * 0.29'
+ pd='2*int((nf+1)/2) * (W/nf + 0.29)' ps='2*int((nf+2)/2) * (W/nf + 0.29)' nrd='0.29 / W' nrs='0.29 / W'
+ sa=0 sb=0 sd=0 mult=1 m=1
XM6 B S Y GND sky130_fd_pr__nfet_01v8 L=0.15 W=1 nf=1 ad='int((nf+1)/2) * W/nf * 0.29' as='int((nf+2)/2) * W/nf * 0.29'
+ pd='2*int((nf+1)/2) * (W/nf + 0.29)' ps='2*int((nf+2)/2) * (W/nf + 0.29)' nrd='0.29 / W' nrs='0.29 / W'
+ sa=0 sb=0 sd=0 mult=1 m=1
.ends

.GLOBAL GND
.GLOBAL VDD
.end
